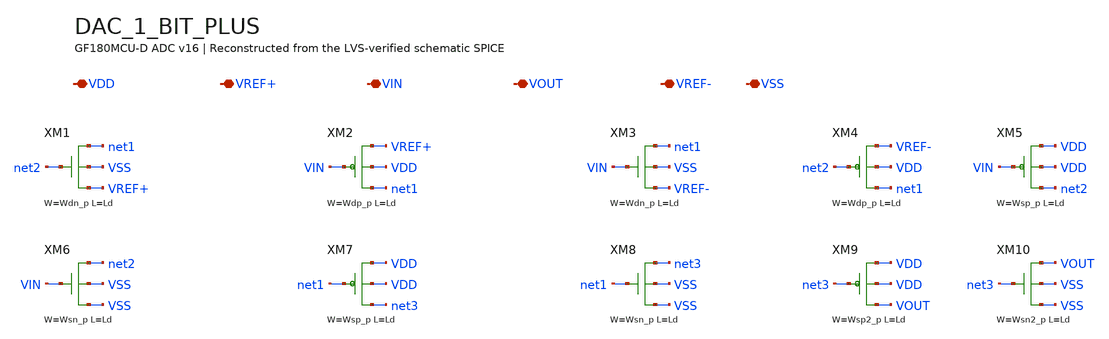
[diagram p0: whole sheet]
** sch_path: src/schematics/INTEGRATION/ADC_final/ADC_v17_Xschem/DAC_1_BIT_PLUS.sch
* Copyright (C) 1998-2026 Stefan Frederik Schippers
* This program is free software; you can redistribute it and/or modify
* it under the terms of the GNU General Public License as published by
* the Free Software Foundation; either version 2 of the License, or
* (at your option) any later version.
**.subckt DAC_1_BIT_PLUS VDD VREF+ VIN VOUT VREF- VSS
*.iopin VDD
*.iopin VREF+
*.iopin VIN
*.iopin VOUT
*.iopin VREF-
*.iopin VSS
XM1 net1 net2 VREF+ VSS nfet_03v3 L=Ld W=Wdn_p nf=2 ad='int((nf+1)/2) * W/nf * 0.18u' as='int((nf+2)/2) * W/nf * 0.18u'
+ pd='2*int((nf+1)/2) * (W/nf + 0.18u)' ps='2*int((nf+2)/2) * (W/nf + 0.18u)' nrd='0.18u / W' nrs='0.18u / W'
+ sa=0 sb=0 sd=0
XM2 net1 VIN VREF+ VDD pfet_03v3 L=Ld W=Wdp_p nf=2 ad='int((nf+1)/2) * W/nf * 0.18u' as='int((nf+2)/2) * W/nf * 0.18u'
+ pd='2*int((nf+1)/2) * (W/nf + 0.18u)' ps='2*int((nf+2)/2) * (W/nf + 0.18u)' nrd='0.18u / W' nrs='0.18u / W'
+ sa=0 sb=0 sd=0
XM3 net1 VIN VREF- VSS nfet_03v3 L=Ld W=Wdn_p nf=2 ad='int((nf+1)/2) * W/nf * 0.18u' as='int((nf+2)/2) * W/nf * 0.18u'
+ pd='2*int((nf+1)/2) * (W/nf + 0.18u)' ps='2*int((nf+2)/2) * (W/nf + 0.18u)' nrd='0.18u / W' nrs='0.18u / W'
+ sa=0 sb=0 sd=0
XM4 net1 net2 VREF- VDD pfet_03v3 L=Ld W=Wdp_p nf=2 ad='int((nf+1)/2) * W/nf * 0.18u' as='int((nf+2)/2) * W/nf * 0.18u'
+ pd='2*int((nf+1)/2) * (W/nf + 0.18u)' ps='2*int((nf+2)/2) * (W/nf + 0.18u)' nrd='0.18u / W' nrs='0.18u / W'
+ sa=0 sb=0 sd=0
XM5 net2 VIN VDD VDD pfet_03v3 L=Ld W=Wsp_p nf=1 ad='int((nf+1)/2) * W/nf * 0.18u' as='int((nf+2)/2) * W/nf * 0.18u'
+ pd='2*int((nf+1)/2) * (W/nf + 0.18u)' ps='2*int((nf+2)/2) * (W/nf + 0.18u)' nrd='0.18u / W' nrs='0.18u / W'
+ sa=0 sb=0 sd=0
XM6 net2 VIN VSS VSS nfet_03v3 L=Ld W=Wsn_p nf=1 ad='int((nf+1)/2) * W/nf * 0.18u' as='int((nf+2)/2) * W/nf * 0.18u'
+ pd='2*int((nf+1)/2) * (W/nf + 0.18u)' ps='2*int((nf+2)/2) * (W/nf + 0.18u)' nrd='0.18u / W' nrs='0.18u / W'
+ sa=0 sb=0 sd=0
XM7 net3 net1 VDD VDD pfet_03v3 L=Ld W=Wsp_p nf=1 ad='int((nf+1)/2) * W/nf * 0.18u' as='int((nf+2)/2) * W/nf * 0.18u'
+ pd='2*int((nf+1)/2) * (W/nf + 0.18u)' ps='2*int((nf+2)/2) * (W/nf + 0.18u)' nrd='0.18u / W' nrs='0.18u / W'
+ sa=0 sb=0 sd=0
XM8 net3 net1 VSS VSS nfet_03v3 L=Ld W=Wsn_p nf=1 ad='int((nf+1)/2) * W/nf * 0.18u' as='int((nf+2)/2) * W/nf * 0.18u'
+ pd='2*int((nf+1)/2) * (W/nf + 0.18u)' ps='2*int((nf+2)/2) * (W/nf + 0.18u)' nrd='0.18u / W' nrs='0.18u / W'
+ sa=0 sb=0 sd=0
XM9 VOUT net3 VDD VDD pfet_03v3 L=Ld W=Wsp2_p nf=1 ad='int((nf+1)/2) * W/nf * 0.18u' as='int((nf+2)/2) * W/nf * 0.18u'
+ pd='2*int((nf+1)/2) * (W/nf + 0.18u)' ps='2*int((nf+2)/2) * (W/nf + 0.18u)' nrd='0.18u / W' nrs='0.18u / W'
+ sa=0 sb=0 sd=0
XM10 VOUT net3 VSS VSS nfet_03v3 L=Ld W=Wsn2_p nf=1 ad='int((nf+1)/2) * W/nf * 0.18u' as='int((nf+2)/2) * W/nf * 0.18u'
+ pd='2*int((nf+1)/2) * (W/nf + 0.18u)' ps='2*int((nf+2)/2) * (W/nf + 0.18u)' nrd='0.18u / W' nrs='0.18u / W'
+ sa=0 sb=0 sd=0
**.ends
.end
